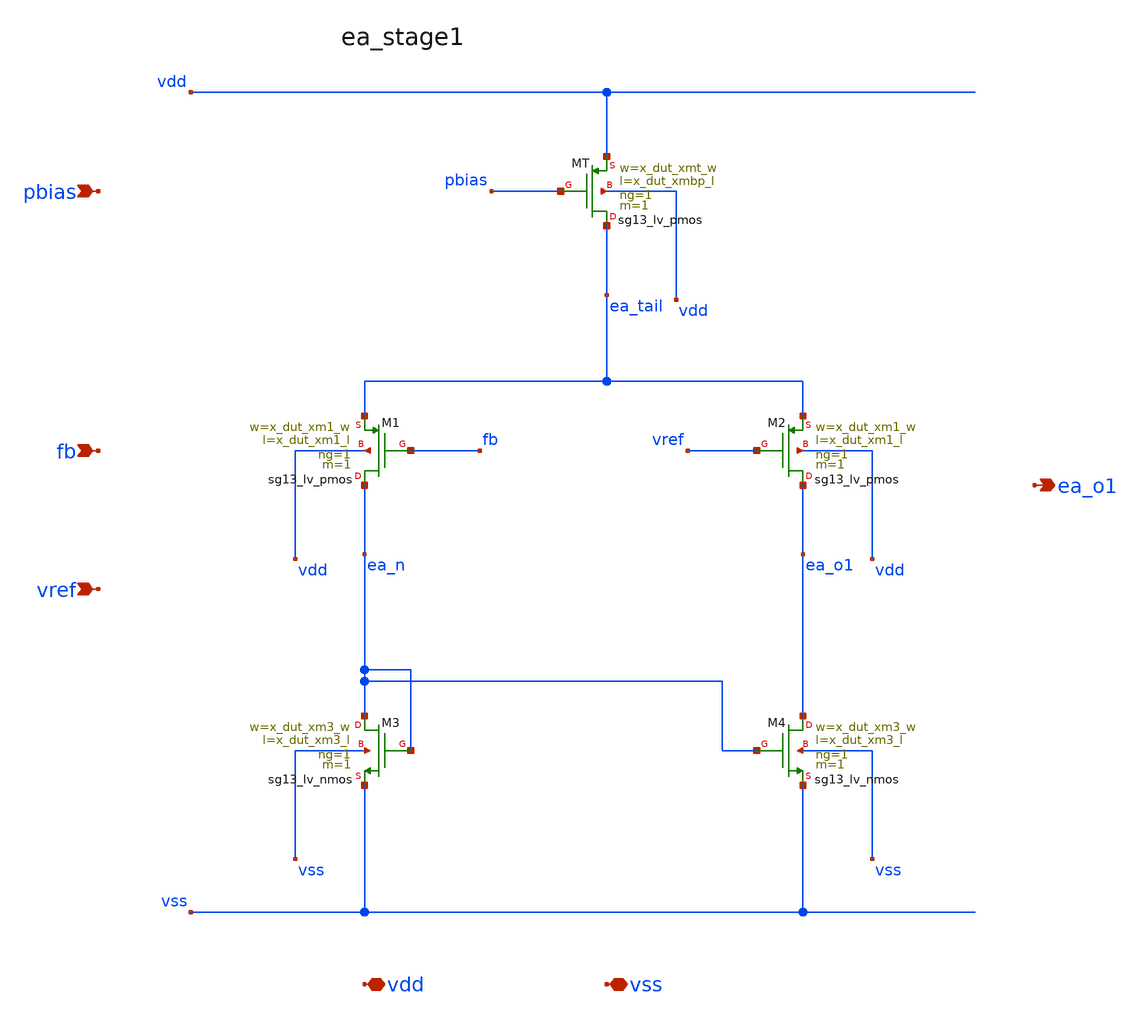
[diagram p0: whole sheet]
** sch_path: circuits/ldo_ihp_capless/xschem/blocks/ea_stage1.sch
**.subckt ea_stage1 pbias fb vref vdd vss ea_o1
*.ipin pbias
*.ipin fb
*.ipin vref
*.iopin vdd
*.iopin vss
*.opin ea_o1
XMT ea_tail pbias vdd vdd sg13_lv_pmos w=x_dut_xmt_w l=x_dut_xmbp_l ng=1 m=1 mm_ok=1
XM1 ea_n fb ea_tail vdd sg13_lv_pmos w=x_dut_xm1_w l=x_dut_xm1_l ng=1 m=1 mm_ok=1
XM2 ea_o1 vref ea_tail vdd sg13_lv_pmos w=x_dut_xm1_w l=x_dut_xm1_l ng=1 m=1 mm_ok=1
XM3 ea_n ea_n vss vss sg13_lv_nmos w=x_dut_xm3_w l=x_dut_xm3_l ng=1 m=1 mm_ok=1
XM4 ea_o1 ea_n vss vss sg13_lv_nmos w=x_dut_xm3_w l=x_dut_xm3_l ng=1 m=1 mm_ok=1
**.ends
.end
